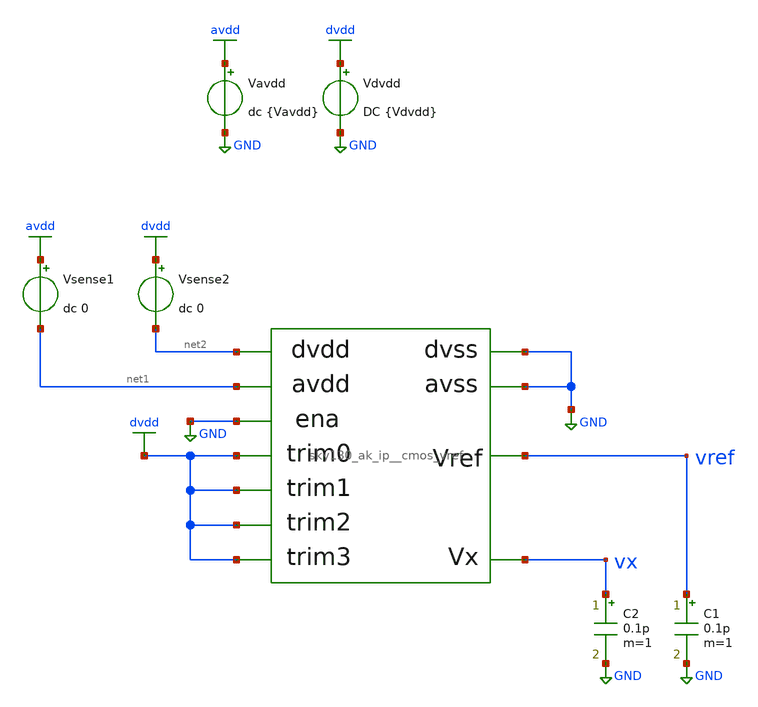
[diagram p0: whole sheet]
** sch_path: cace/tb_vref_mc.sch
**.subckt tb_vref_mc
Vavdd avdd GND dc {Vavdd}
X1 net1 GND dvdd vref vx dvdd dvdd dvdd net2 GND GND sky130_ak_ip__cmos_vref
Vsense1 avdd net1 dc 0
C2 vx GND 0.1p m=1
Vdvdd dvdd GND DC {Vdvdd}
C1 vref GND 0.1p m=1
Vsense2 dvdd net2 dc 0
**** begin user architecture code


.control
set wr_singlescale
let it = 0
let iterations = {iterations|maximum}
let output_option = {output_option}
let vref_data = vector(iterations)
let vref_mean = 0
print iterations
print vref_data
dowhile it < iterations
	reset
	op
	let vref_data[it] = V(vref)
	let vref_mean = vref_mean + V(vref)
	let it = it + 1
end
if output_option = 0
	print V(vref_data)
	let it = 1
	wrdata ngspice/test.data vref_data[0]
	set appendwrite
	dowhile it < iterations
		wrdata {simpath}/{filename}_{N}.data vref_data[it]
		let it = it + 1
	end
	quit
end
let vref_mean = vref_mean / iterations
if output_option = 1
	print vref_mean
	wrdata {simpath}/{filename}_{N}.data vref_mean
	quit
end
let vref_deviation = 0
let it = 0;
dowhile it < iterations
	let vref_deviation = vref_deviation + (vref_data[it]-vref_mean)^2
	let it = it+1
end
let vref_deviation = (vref_deviation / iterations)^0.5
let vref_accuracy = 3 * vref_deviation / vref_mean
print vref_accuracy
wrdata {simpath}/{filename}_{N}.data vref_accuracy
quit
.endc




.lib /usr/local/share/pdk/sky130A/libs.tech/combined/sky130.lib.spice mc
.option TEMP={temperature}
.option warn=1


**** end user architecture code
**.ends

* expanding   symbol:  /home/moduhub/work/sky130_ak_ip__cmos_vref/xschem/sky130_ak_ip__cmos_vref.sym
*+ # of pins=11
** sym_path: xschem/sky130_ak_ip__cmos_vref.sym
** sch_path: xschem/sky130_ak_ip__cmos_vref.sch
.subckt sky130_ak_ip__cmos_vref avdd avss trim0 vref vx trim1 trim2 trim3 dvdd dvss ena
*.opin vref
*.iopin avss
*.iopin avdd
*.opin vx
*.ipin trim0
*.ipin trim1
*.ipin trim2
*.ipin trim3
*.iopin dvdd
*.iopin dvss
*.iopin avdd
*.ipin ena
XM3 net1 net3 vx GND sky130_fd_pr__nfet_g5v0d10v5 L=1 W=100 nf=5 ad='int((nf+1)/2) * W/nf * 0.29' as='int((nf+2)/2) * W/nf * 0.29'
+ pd='2*int((nf+1)/2) * (W/nf + 0.29)' ps='2*int((nf+2)/2) * (W/nf + 0.29)' nrd='0.29 / W' nrs='0.29 / W'
+ sa=0 sb=0 sd=0 mult=1 m=1
XM4 net2 net3 avss GND sky130_fd_pr__nfet_g5v0d10v5 L=1 W=5 nf=1 ad='int((nf+1)/2) * W/nf * 0.29' as='int((nf+2)/2) * W/nf * 0.29'
+ pd='2*int((nf+1)/2) * (W/nf + 0.29)' ps='2*int((nf+2)/2) * (W/nf + 0.29)' nrd='0.29 / W' nrs='0.29 / W'
+ sa=0 sb=0 sd=0 mult=1 m=1
XM5 net4 vref net1 GND sky130_fd_pr__nfet_g5v0d10v5 L=10 W=10 nf=1 ad='int((nf+1)/2) * W/nf * 0.29' as='int((nf+2)/2) * W/nf * 0.29'
+ pd='2*int((nf+1)/2) * (W/nf + 0.29)' ps='2*int((nf+2)/2) * (W/nf + 0.29)' nrd='0.29 / W' nrs='0.29 / W'
+ sa=0 sb=0 sd=0 mult=1 m=1
XM6 net3 vref net2 GND sky130_fd_pr__nfet_g5v0d10v5 L=10 W=10 nf=1 ad='int((nf+1)/2) * W/nf * 0.29' as='int((nf+2)/2) * W/nf * 0.29'
+ pd='2*int((nf+1)/2) * (W/nf + 0.29)' ps='2*int((nf+2)/2) * (W/nf + 0.29)' nrd='0.29 / W' nrs='0.29 / W'
+ sa=0 sb=0 sd=0 mult=1 m=1
XM7 net4 net4 avdd_ena avdd sky130_fd_pr__pfet_g5v0d10v5 L=10 W=5 nf=1 ad='int((nf+1)/2) * W/nf * 0.29'
+ as='int((nf+2)/2) * W/nf * 0.29' pd='2*int((nf+1)/2) * (W/nf + 0.29)' ps='2*int((nf+2)/2) * (W/nf + 0.29)'
+ nrd='0.29 / W' nrs='0.29 / W' sa=0 sb=0 sd=0 mult=1 m=1
XM8 net3 net4 avdd_ena avdd sky130_fd_pr__pfet_g5v0d10v5 L=10 W=5 nf=1 ad='int((nf+1)/2) * W/nf * 0.29'
+ as='int((nf+2)/2) * W/nf * 0.29' pd='2*int((nf+1)/2) * (W/nf + 0.29)' ps='2*int((nf+2)/2) * (W/nf + 0.29)'
+ nrd='0.29 / W' nrs='0.29 / W' sa=0 sb=0 sd=0 mult=1 m=1
XM9 vref net4 avdd_ena avdd sky130_fd_pr__pfet_g5v0d10v5 L=10 W=50 nf=1 ad='int((nf+1)/2) * W/nf * 0.29'
+ as='int((nf+2)/2) * W/nf * 0.29' pd='2*int((nf+1)/2) * (W/nf + 0.29)' ps='2*int((nf+2)/2) * (W/nf + 0.29)'
+ nrd='0.29 / W' nrs='0.29 / W' sa=0 sb=0 sd=0 mult=1 m=1
XM10 net5 net3 avss GND sky130_fd_pr__nfet_g5v0d10v5 L=1 W=5 nf=1 ad='int((nf+1)/2) * W/nf * 0.29' as='int((nf+2)/2) * W/nf * 0.29'
+ pd='2*int((nf+1)/2) * (W/nf + 0.29)' ps='2*int((nf+2)/2) * (W/nf + 0.29)' nrd='0.29 / W' nrs='0.29 / W'
+ sa=0 sb=0 sd=0 mult=1 m=1
XM11 net4 net5 avss GND sky130_fd_pr__nfet_g5v0d10v5 L=1 W=5 nf=1 ad='int((nf+1)/2) * W/nf * 0.29' as='int((nf+2)/2) * W/nf * 0.29'
+ pd='2*int((nf+1)/2) * (W/nf + 0.29)' ps='2*int((nf+2)/2) * (W/nf + 0.29)' nrd='0.29 / W' nrs='0.29 / W'
+ sa=0 sb=0 sd=0 mult=1 m=1
XC1 avdd_ena net5 sky130_fd_pr__cap_mim_m3_1 W=5 L=5 MF=1 m=1
XM12 vref net4 net9 avdd sky130_fd_pr__pfet_g5v0d10v5 L=10 W=1 nf=1 ad='int((nf+1)/2) * W/nf * 0.29'
+ as='int((nf+2)/2) * W/nf * 0.29' pd='2*int((nf+1)/2) * (W/nf + 0.29)' ps='2*int((nf+2)/2) * (W/nf + 0.29)'
+ nrd='0.29 / W' nrs='0.29 / W' sa=0 sb=0 sd=0 mult=1 m=1
XM13 vref net4 net8 avdd sky130_fd_pr__pfet_g5v0d10v5 L=10 W=2 nf=1 ad='int((nf+1)/2) * W/nf * 0.29'
+ as='int((nf+2)/2) * W/nf * 0.29' pd='2*int((nf+1)/2) * (W/nf + 0.29)' ps='2*int((nf+2)/2) * (W/nf + 0.29)'
+ nrd='0.29 / W' nrs='0.29 / W' sa=0 sb=0 sd=0 mult=1 m=1
XM14 net9 trim0 avdd_ena dvdd sky130_fd_pr__pfet_g5v0d10v5 L=0.15 W=1 nf=1 ad='int((nf+1)/2) * W/nf * 0.29'
+ as='int((nf+2)/2) * W/nf * 0.29' pd='2*int((nf+1)/2) * (W/nf + 0.29)' ps='2*int((nf+2)/2) * (W/nf + 0.29)'
+ nrd='0.29 / W' nrs='0.29 / W' sa=0 sb=0 sd=0 mult=1 m=1
XM15 net8 trim1 avdd_ena dvdd sky130_fd_pr__pfet_g5v0d10v5 L=0.15 W=1 nf=1 ad='int((nf+1)/2) * W/nf * 0.29'
+ as='int((nf+2)/2) * W/nf * 0.29' pd='2*int((nf+1)/2) * (W/nf + 0.29)' ps='2*int((nf+2)/2) * (W/nf + 0.29)'
+ nrd='0.29 / W' nrs='0.29 / W' sa=0 sb=0 sd=0 mult=1 m=1
XM16 vref net4 net7 avdd sky130_fd_pr__pfet_g5v0d10v5 L=10 W=4 nf=1 ad='int((nf+1)/2) * W/nf * 0.29'
+ as='int((nf+2)/2) * W/nf * 0.29' pd='2*int((nf+1)/2) * (W/nf + 0.29)' ps='2*int((nf+2)/2) * (W/nf + 0.29)'
+ nrd='0.29 / W' nrs='0.29 / W' sa=0 sb=0 sd=0 mult=1 m=1
XM17 net7 trim2 avdd_ena dvdd sky130_fd_pr__pfet_g5v0d10v5 L=0.15 W=1 nf=1 ad='int((nf+1)/2) * W/nf * 0.29'
+ as='int((nf+2)/2) * W/nf * 0.29' pd='2*int((nf+1)/2) * (W/nf + 0.29)' ps='2*int((nf+2)/2) * (W/nf + 0.29)'
+ nrd='0.29 / W' nrs='0.29 / W' sa=0 sb=0 sd=0 mult=1 m=1
XM18 vref net4 net6 avdd sky130_fd_pr__pfet_g5v0d10v5 L=10 W=8 nf=1 ad='int((nf+1)/2) * W/nf * 0.29'
+ as='int((nf+2)/2) * W/nf * 0.29' pd='2*int((nf+1)/2) * (W/nf + 0.29)' ps='2*int((nf+2)/2) * (W/nf + 0.29)'
+ nrd='0.29 / W' nrs='0.29 / W' sa=0 sb=0 sd=0 mult=1 m=1
XM19 net6 trim3 avdd_ena dvdd sky130_fd_pr__pfet_g5v0d10v5 L=0.15 W=1 nf=1 ad='int((nf+1)/2) * W/nf * 0.29'
+ as='int((nf+2)/2) * W/nf * 0.29' pd='2*int((nf+1)/2) * (W/nf + 0.29)' ps='2*int((nf+2)/2) * (W/nf + 0.29)'
+ nrd='0.29 / W' nrs='0.29 / W' sa=0 sb=0 sd=0 mult=1 m=1
XM1 vx vref avss GND sky130_fd_pr__nfet_g5v0d10v5 L=10 W=2.5 nf=1 ad='int((nf+1)/2) * W/nf * 0.29' as='int((nf+2)/2) * W/nf * 0.29'
+ pd='2*int((nf+1)/2) * (W/nf + 0.29)' ps='2*int((nf+2)/2) * (W/nf + 0.29)' nrd='0.29 / W' nrs='0.29 / W'
+ sa=0 sb=0 sd=0 mult=1 m=1
XM2 vref vref vx GND sky130_fd_pr__nfet_g5v0d10v5 L=10 W=2 nf=1 ad='int((nf+1)/2) * W/nf * 0.29' as='int((nf+2)/2) * W/nf * 0.29'
+ pd='2*int((nf+1)/2) * (W/nf + 0.29)' ps='2*int((nf+2)/2) * (W/nf + 0.29)' nrd='0.29 / W' nrs='0.29 / W'
+ sa=0 sb=0 sd=0 mult=1 m=1
XM20 avdd_ena ena avdd dvdd sky130_fd_pr__pfet_g5v0d10v5 L=0.3 W=5 nf=1 ad='int((nf+1)/2) * W/nf * 0.29'
+ as='int((nf+2)/2) * W/nf * 0.29' pd='2*int((nf+1)/2) * (W/nf + 0.29)' ps='2*int((nf+2)/2) * (W/nf + 0.29)'
+ nrd='0.29 / W' nrs='0.29 / W' sa=0 sb=0 sd=0 mult=1 m=1
.ends

.GLOBAL avdd
.GLOBAL GND
.GLOBAL dvdd
.end
